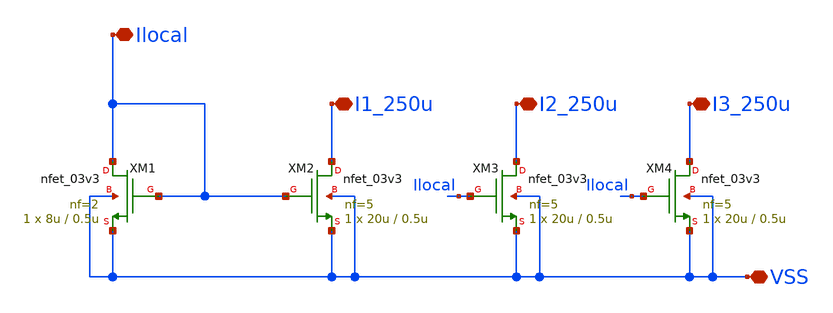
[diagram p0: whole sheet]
** sch_path: designs/mirrors/schematic/nmos_mirror.sch
**.subckt nmos_mirror VSS Ilocal I1_250u I2_250u I3_250u
*.iopin VSS
*.iopin Ilocal
*.iopin I1_250u
*.iopin I2_250u
*.iopin I3_250u
XM1 Ilocal Ilocal VSS VSS nfet_03v3 L=0.5u W=8u nf=2 ad='int((nf+1)/2) * W/nf * 0.18u' as='int((nf+2)/2) * W/nf * 0.18u'
+ pd='2*int((nf+1)/2) * (W/nf + 0.18u)' ps='2*int((nf+2)/2) * (W/nf + 0.18u)' nrd='0.18u / W' nrs='0.18u / W'
+ sa=0 sb=0 sd=0 m=1
XM2 I1_250u Ilocal VSS VSS nfet_03v3 L=0.5u W=20u nf=5 ad='int((nf+1)/2) * W/nf * 0.18u' as='int((nf+2)/2) * W/nf * 0.18u'
+ pd='2*int((nf+1)/2) * (W/nf + 0.18u)' ps='2*int((nf+2)/2) * (W/nf + 0.18u)' nrd='0.18u / W' nrs='0.18u / W'
+ sa=0 sb=0 sd=0 m=1
XM3 I2_250u Ilocal VSS VSS nfet_03v3 L=0.5u W=20u nf=5 ad='int((nf+1)/2) * W/nf * 0.18u' as='int((nf+2)/2) * W/nf * 0.18u'
+ pd='2*int((nf+1)/2) * (W/nf + 0.18u)' ps='2*int((nf+2)/2) * (W/nf + 0.18u)' nrd='0.18u / W' nrs='0.18u / W'
+ sa=0 sb=0 sd=0 m=1
XM4 I3_250u Ilocal VSS VSS nfet_03v3 L=0.5u W=20u nf=5 ad='int((nf+1)/2) * W/nf * 0.18u' as='int((nf+2)/2) * W/nf * 0.18u'
+ pd='2*int((nf+1)/2) * (W/nf + 0.18u)' ps='2*int((nf+2)/2) * (W/nf + 0.18u)' nrd='0.18u / W' nrs='0.18u / W'
+ sa=0 sb=0 sd=0 m=1
**.ends
.end
